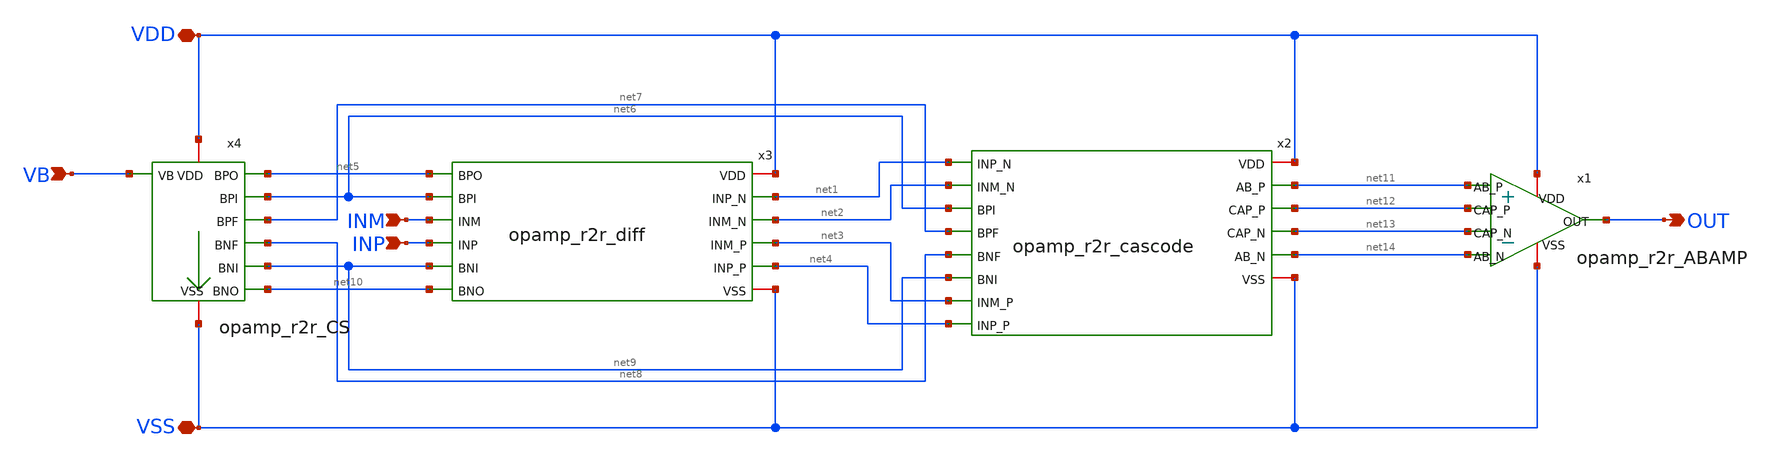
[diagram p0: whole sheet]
** sch_path: OpenSUSI-TR10/opamp_r2r_audio/opamp_r2r.sch
**.subckt opamp_r2r OUT VDD VSS VB INM INP
*.opin OUT
*.iopin VDD
*.iopin VSS
*.ipin VB
*.ipin INM
*.ipin INP
x1 net11 net12 net13 net14 VDD OUT VSS opamp_r2r_ABAMP
x2 VDD net1 net2 net6 net11 net7 net12 net13 net8 net14 net9 net3 net4 VSS opamp_r2r_cascode
x3 VDD net5 net1 net2 net6 INM INP net9 net3 net4 net10 VSS opamp_r2r_diff
x4 VDD net5 net6 net7 VB net8 net9 net10 VSS opamp_r2r_CS
**.ends

* expanding   symbol:  opamp_r2r_ABAMP.sym # of pins=7
** sym_path: OpenSUSI-TR10/opamp_r2r_audio/opamp_r2r_ABAMP.sym
** sch_path: OpenSUSI-TR10/opamp_r2r_audio/opamp_r2r_ABAMP.sch
.subckt opamp_r2r_ABAMP AB_P CAP_P CAP_N AB_N VDD OUT VSS
*.iopin VDD
*.iopin VSS
*.opin OUT
*.ipin AB_P
*.ipin AB_N
*.ipin CAP_P
*.ipin CAP_N
XMDRVP OUT AB_P VDD VDD PMOS w=6u l=4u as=0 ad=0 ps=0 pd=0 nrd=0 nrs=0 m=96
XMDRVN OUT AB_N VSS VSS NMOS w=6u l=4u as=0 ad=0 ps=0 pd=0 nrd=0 nrs=0 m=48
XXCP2 CAP_P OUT VSS F_CSIO c=3.898p x=80.6u y=80.6u m=1
XXCP1 CAP_P OUT VSS F_CSIO c=3.898p x=80.6u y=80.6u m=1
XXCN2 CAP_N OUT VSS F_CSIO c=3.898p x=80.6u y=80.6u m=1
XXCN1 CAP_N OUT VSS F_CSIO c=3.898p x=80.6u y=80.6u m=1
.ends


* expanding   symbol:  opamp_r2r_cascode.sym # of pins=14
** sym_path: OpenSUSI-TR10/opamp_r2r_audio/opamp_r2r_cascode.sym
** sch_path: OpenSUSI-TR10/opamp_r2r_audio/opamp_r2r_cascode.sch
.subckt opamp_r2r_cascode VDD INP_N INM_N BPI AB_P BPF CAP_P CAP_N BNF AB_N BNI INM_P INP_P VSS
*.iopin VDD
*.iopin VSS
*.ipin INP_N
*.opin AB_P
*.opin AB_N
*.opin CAP_P
*.opin CAP_N
*.ipin INM_N
*.ipin INM_P
*.ipin INP_P
*.ipin BPI
*.ipin BPF
*.ipin BNF
*.ipin BNI
XMCSMP1 INM_N net1 VDD VDD PMOS w=6u l=4u as=0 ad=0 ps=0 pd=0 nrd=0 nrs=0 m=16
XMCSMP2 net1 BPI INM_N VDD PMOS w=6u l=4u as=0 ad=0 ps=0 pd=0 nrd=0 nrs=0 m=8
XMCSMP3 net2 BPF net1 VDD PMOS w=6u l=4u as=0 ad=0 ps=0 pd=0 nrd=0 nrs=0 m=4
XMCSPP1 INP_N net1 VDD VDD PMOS w=6u l=4u as=0 ad=0 ps=0 pd=0 nrd=0 nrs=0 m=16
XMCSPP2 AB_P BPI INP_N VDD PMOS w=6u l=4u as=0 ad=0 ps=0 pd=0 nrd=0 nrs=0 m=8
XMCSPP3 AB_N BPF AB_P VDD PMOS w=6u l=4u as=0 ad=0 ps=0 pd=0 nrd=0 nrs=0 m=4
XMCSMN2 net2 BNI INM_P VSS NMOS w=6u l=4u as=0 ad=0 ps=0 pd=0 nrd=0 nrs=0 m=4
XMCSMN1 INM_P net2 VSS VSS NMOS w=6u l=4u as=0 ad=0 ps=0 pd=0 nrd=0 nrs=0 m=8
XMCSMN3 net1 BNF net2 VSS NMOS w=6u l=4u as=0 ad=0 ps=0 pd=0 nrd=0 nrs=0 m=2
XMCSPN3 AB_P BNF AB_N VSS NMOS w=6u l=4u as=0 ad=0 ps=0 pd=0 nrd=0 nrs=0 m=2
XMCSPN2 AB_N BNI INP_P VSS NMOS w=6u l=4u as=0 ad=0 ps=0 pd=0 nrd=0 nrs=0 m=4
XMCSPN1 INP_P net2 VSS VSS NMOS w=6u l=4u as=0 ad=0 ps=0 pd=0 nrd=0 nrs=0 m=8
XMSBPN2 net4 net4 net3 VSS NMOS w=6u l=4u as=0 ad=0 ps=0 pd=0 nrd=0 nrs=0 m=2
XMSBPN1 net3 net3 VSS VSS NMOS w=6u l=4u as=0 ad=0 ps=0 pd=0 nrd=0 nrs=0 m=2
XMSBPP1 net4 AB_P VDD VDD PMOS w=6u l=4u as=0 ad=0 ps=0 pd=0 nrd=0 nrs=0 m=4
XMSBNP1 net5 net5 VDD VDD PMOS w=6u l=4u as=0 ad=0 ps=0 pd=0 nrd=0 nrs=0 m=4
XMSBNP2 net6 net6 net5 VDD PMOS w=6u l=4u as=0 ad=0 ps=0 pd=0 nrd=0 nrs=0 m=4
XMSBNN1 net6 AB_N VSS VSS NMOS w=6u l=4u as=0 ad=0 ps=0 pd=0 nrd=0 nrs=0 m=2
XMSBNP3 CAP_P net6 INP_N VDD PMOS w=6u l=4u as=0 ad=0 ps=0 pd=0 nrd=0 nrs=0 m=16
XMSBPN3 CAP_N net4 INP_P VSS NMOS w=6u l=4u as=0 ad=0 ps=0 pd=0 nrd=0 nrs=0 m=8
XMSBPDMYN INP_P VSS VSS VSS NMOS w=6u l=4u as=0 ad=0 ps=0 pd=0 nrd=0 nrs=0 m=2
XMSBNDMYP INP_N VDD VDD VDD PMOS w=6u l=4u as=0 ad=0 ps=0 pd=0 nrd=0 nrs=0 m=4
XMDMYN1 VSS VSS VSS VSS NMOS w=6u l=4u as=0 ad=0 ps=0 pd=0 nrd=0 nrs=0 m=22
XMDMYP1 VDD VDD VDD VDD PMOS w=6u l=4u as=0 ad=0 ps=0 pd=0 nrd=0 nrs=0 m=52
XMDMYP2 BNO VDD VDD VDD PMOS w=6u l=4u as=0 ad=0 ps=0 pd=0 nrd=0 nrs=0 m=2
XMDMYP3 BNI VDD VDD VDD PMOS w=6u l=4u as=0 ad=0 ps=0 pd=0 nrd=0 nrs=0 m=2
XMCSMDMYP net2 VDD net1 VDD PMOS w=6u l=4u as=0 ad=0 ps=0 pd=0 nrd=0 nrs=0 m=4
XMCSPDMYP AB_N VDD AB_P VDD PMOS w=6u l=4u as=0 ad=0 ps=0 pd=0 nrd=0 nrs=0 m=4
XMCSMDMYN net1 VSS net2 VSS NMOS w=6u l=4u as=0 ad=0 ps=0 pd=0 nrd=0 nrs=0 m=2
XMCSPDMYN AB_P VSS AB_N VSS NMOS w=6u l=4u as=0 ad=0 ps=0 pd=0 nrd=0 nrs=0 m=2
.ends


* expanding   symbol:  opamp_r2r_diff.sym # of pins=12
** sym_path: OpenSUSI-TR10/opamp_r2r_audio/opamp_r2r_diff.sym
** sch_path: OpenSUSI-TR10/opamp_r2r_audio/opamp_r2r_diff.sch
.subckt opamp_r2r_diff VDD BPO INP_N INM_N BPI INM INP BNI INM_P INP_P BNO VSS
*.iopin VDD
*.iopin VSS
*.ipin INP
*.ipin INM
*.opin INP_N
*.opin INM_N
*.opin INM_P
*.opin INP_P
*.ipin BPO
*.ipin BPI
*.ipin BNI
*.ipin BNO
XMINPP1 net1 BPO VDD VDD PMOS w=6u l=4u as=0 ad=0 ps=0 pd=0 nrd=0 nrs=0 m=8
XMINPP2 net2 BPI net1 VDD PMOS w=6u l=4u as=0 ad=0 ps=0 pd=0 nrd=0 nrs=0 m=8
XMINPP3 INP_P INP net2 VDD PMOS w=6u l=4u as=0 ad=0 ps=0 pd=0 nrd=0 nrs=0 m=8
XMINMP1 net3 BPO VDD VDD PMOS w=6u l=4u as=0 ad=0 ps=0 pd=0 nrd=0 nrs=0 m=8
XMINMP2 net2 BPI net3 VDD PMOS w=6u l=4u as=0 ad=0 ps=0 pd=0 nrd=0 nrs=0 m=8
XMINMP3 INM_P INM net2 VDD PMOS w=6u l=4u as=0 ad=0 ps=0 pd=0 nrd=0 nrs=0 m=8
XMINPN2 net4 BNI net5 VSS NMOS w=6u l=4u as=0 ad=0 ps=0 pd=0 nrd=0 nrs=0 m=4
XMINPN1 net5 BNO VSS VSS NMOS w=6u l=4u as=0 ad=0 ps=0 pd=0 nrd=0 nrs=0 m=4
XMINPN3 INP_N INP net4 VSS NMOS w=6u l=4u as=0 ad=0 ps=0 pd=0 nrd=0 nrs=0 m=4
XMINMN2 net4 BNI net6 VSS NMOS w=6u l=4u as=0 ad=0 ps=0 pd=0 nrd=0 nrs=0 m=4
XMINMN1 net6 BNO VSS VSS NMOS w=6u l=4u as=0 ad=0 ps=0 pd=0 nrd=0 nrs=0 m=4
XMINMN3 INM_N INM net4 VSS NMOS w=6u l=4u as=0 ad=0 ps=0 pd=0 nrd=0 nrs=0 m=4
.ends


* expanding   symbol:  opamp_r2r_CS.sym # of pins=9
** sym_path: OpenSUSI-TR10/opamp_r2r_audio/opamp_r2r_CS.sym
** sch_path: OpenSUSI-TR10/opamp_r2r_audio/opamp_r2r_CS.sch
.subckt opamp_r2r_CS VDD BPO BPI BPF VB BNF BNI BNO VSS
*.iopin VDD
*.iopin VSS
*.ipin VB
*.opin BPO
*.opin BPI
*.opin BPF
*.opin BNF
*.opin BNI
*.opin BNO
XMB4P1 net1 BPO VDD VDD PMOS w=6u l=4u as=0 ad=0 ps=0 pd=0 nrd=0 nrs=0 m=4
XMB4P2 BPO BPI net1 VDD PMOS w=6u l=4u as=0 ad=0 ps=0 pd=0 nrd=0 nrs=0 m=4
XMB3P1 net2 BPI VDD VDD PMOS w=6u l=4u as=0 ad=0 ps=0 pd=0 nrd=0 nrs=0 m=2
XMB3P2 net3 BPI net2 VDD PMOS w=6u l=4u as=0 ad=0 ps=0 pd=0 nrd=0 nrs=0 m=2
XMB3P3 BPI BPI net3 VDD PMOS w=6u l=4u as=0 ad=0 ps=0 pd=0 nrd=0 nrs=0 m=2
XMB4N2 BPO BNI net4 VSS NMOS w=6u l=4u as=0 ad=0 ps=0 pd=0 nrd=0 nrs=0 m=2
XMB3N2 BPI BNI net5 VSS NMOS w=6u l=4u as=0 ad=0 ps=0 pd=0 nrd=0 nrs=0 m=2
XMB4N1 net4 BNO VSS VSS NMOS w=6u l=4u as=0 ad=0 ps=0 pd=0 nrd=0 nrs=0 m=2
XMB3N1 net5 BNO VSS VSS NMOS w=6u l=4u as=0 ad=0 ps=0 pd=0 nrd=0 nrs=0 m=2
XMB1N2 BNO BNI net7 VSS NMOS w=6u l=4u as=0 ad=0 ps=0 pd=0 nrd=0 nrs=0 m=2
XMB2N2 net6 BNI net8 VSS NMOS w=6u l=4u as=0 ad=0 ps=0 pd=0 nrd=0 nrs=0 m=1
XMB1N1 net7 BNO VSS VSS NMOS w=6u l=4u as=0 ad=0 ps=0 pd=0 nrd=0 nrs=0 m=2
XMB2N1 net8 BNI VSS VSS NMOS w=6u l=4u as=0 ad=0 ps=0 pd=0 nrd=0 nrs=0 m=1
XMB2N3 BNI BNI net6 VSS NMOS w=6u l=4u as=0 ad=0 ps=0 pd=0 nrd=0 nrs=0 m=1
XMB5P1 net9 BPO VDD VDD PMOS w=6u l=4u as=0 ad=0 ps=0 pd=0 nrd=0 nrs=0 m=4
XMB5P2 BNF BPI net9 VDD PMOS w=6u l=4u as=0 ad=0 ps=0 pd=0 nrd=0 nrs=0 m=4
XMB5N2 net10 BNI net11 VSS NMOS w=6u l=4u as=0 ad=0 ps=0 pd=0 nrd=0 nrs=0 m=2
XMB5N1 net11 net10 VSS VSS NMOS w=6u l=4u as=0 ad=0 ps=0 pd=0 nrd=0 nrs=0 m=2
XMB5N3 BNF BNF net10 VSS NMOS w=6u l=4u as=0 ad=0 ps=0 pd=0 nrd=0 nrs=0 m=2
XMB6P1 net12 net14 VDD VDD PMOS w=6u l=4u as=0 ad=0 ps=0 pd=0 nrd=0 nrs=0 m=4
XMB6P2 net14 BPI net12 VDD PMOS w=6u l=4u as=0 ad=0 ps=0 pd=0 nrd=0 nrs=0 m=4
XMB6N2 BPF BNI net13 VSS NMOS w=6u l=4u as=0 ad=0 ps=0 pd=0 nrd=0 nrs=0 m=2
XMB6N1 net13 BNO VSS VSS NMOS w=6u l=4u as=0 ad=0 ps=0 pd=0 nrd=0 nrs=0 m=2
XMB6P3 BPF BPF net14 VDD PMOS w=6u l=4u as=0 ad=0 ps=0 pd=0 nrd=0 nrs=0 m=4
XMB2DMYN BNI VSS VSS VSS NMOS w=6u l=4u as=0 ad=0 ps=0 pd=0 nrd=0 nrs=0 m=1
XMDMYN1 VSS VSS VSS VSS NMOS w=6u l=4u as=0 ad=0 ps=0 pd=0 nrd=0 nrs=0 m=22
XMDMYP1 VDD VDD VDD VDD PMOS w=6u l=4u as=0 ad=0 ps=0 pd=0 nrd=0 nrs=0 m=52
XMPVB1 BNI VB VDD VDD PMOS w=6u l=4u as=0 ad=0 ps=0 pd=0 nrd=0 nrs=0 m=2
XMPVB2 BNO VB VDD VDD PMOS w=6u l=4u as=0 ad=0 ps=0 pd=0 nrd=0 nrs=0 m=2
XMDMYP2 BNO VDD VDD VDD PMOS w=6u l=4u as=0 ad=0 ps=0 pd=0 nrd=0 nrs=0 m=2
XMDMYP3 BNI VDD VDD VDD PMOS w=6u l=4u as=0 ad=0 ps=0 pd=0 nrd=0 nrs=0 m=2
XMDMYP4 BPI VDD VDD VDD PMOS w=6u l=4u as=0 ad=0 ps=0 pd=0 nrd=0 nrs=0 m=2
.ends

.end
